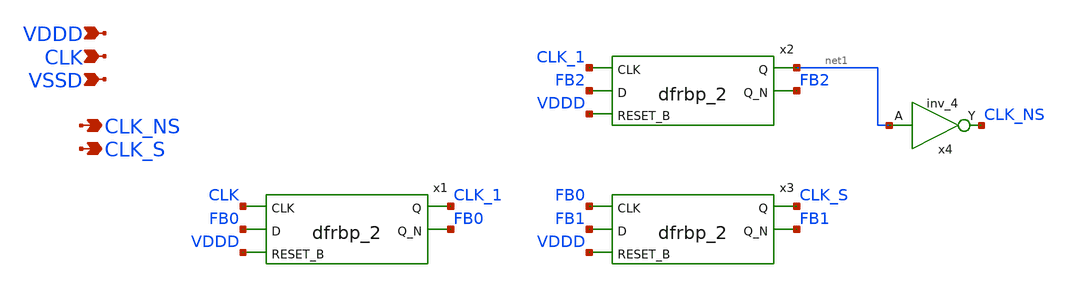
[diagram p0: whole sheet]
** sch_path: top/ckc_shifter.sch
**.subckt ckc_shifter CLK VDDD VSSD CLK_NS CLK_S
*.ipin CLK
*.ipin VDDD
*.ipin VSSD
*.opin CLK_NS
*.opin CLK_S
x1 CLK FB0 VDDD VSSD VSSD VDDD VDDD CLK_1 FB0 sky130_fd_sc_hd__dfrbp_2
x2 CLK_1 FB2 VDDD VSSD VSSD VDDD VDDD net1 FB2 sky130_fd_sc_hd__dfrbp_2
x3 FB0 FB1 VDDD VSSD VSSD VDDD VDDD CLK_S FB1 sky130_fd_sc_hd__dfrbp_2
x4 net1 VSSD VSSD VDDD VDDD CLK_NS sky130_fd_sc_hd__inv_4
**.ends
.end
